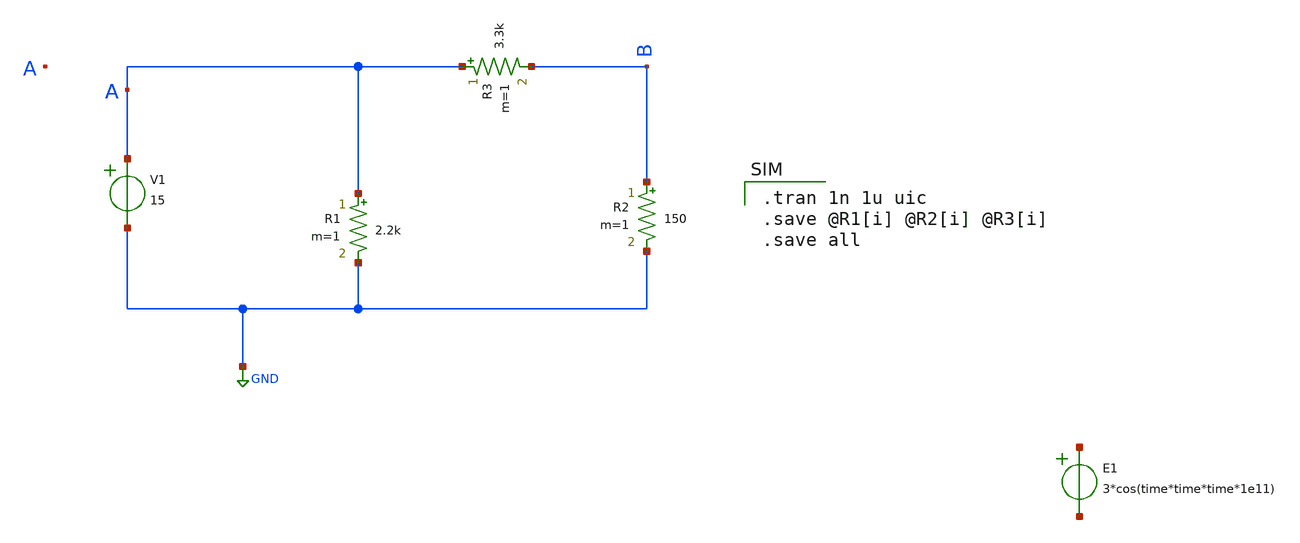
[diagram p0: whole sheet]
** sch_path: Bai2.sch
**.subckt Bai2
R1 A GND 2.2k m=1
R2 B GND 150 m=1
R3 A B 3.3k m=1
E1 net1 net2 VOL=' 3*cos(time*time*time*1e11) '
V1 A GND VOL=' 15 '
**** begin user architecture code

.tran 1n 1u uic
.save @R1[i] @R2[i] @R3[i]
.save all

**** end user architecture code
**.ends
.GLOBAL GND
.end
